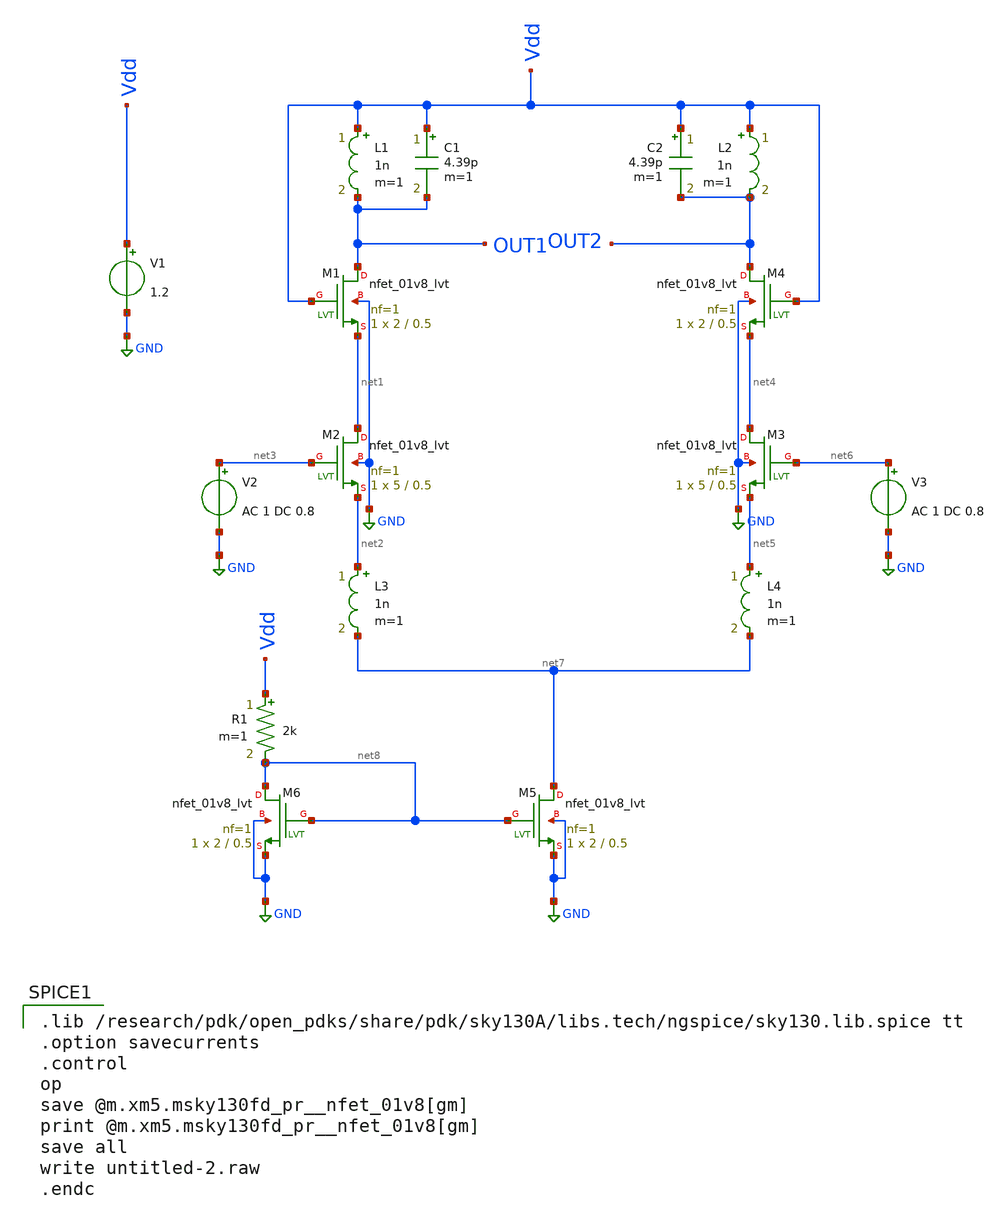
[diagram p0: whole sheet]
** sch_path: skywater_stuff/ECE631_RF_CMOS/untitled-2.sch
**.subckt untitled-2
XM1 OUT1 Vdd net1 GND sky130_fd_pr__nfet_01v8_lvt L=0.5 W=2 nf=1 ad='int((nf+1)/2) * W/nf * 0.29' as='int((nf+2)/2) * W/nf * 0.29'
+ pd='2*int((nf+1)/2) * (W/nf + 0.29)' ps='2*int((nf+2)/2) * (W/nf + 0.29)' nrd='0.29 / W' nrs='0.29 / W'
+ sa=0 sb=0 sd=0 mult=1 m=1
XM2 net1 net3 net2 GND sky130_fd_pr__nfet_01v8_lvt L=0.5 W=5 nf=1 ad='int((nf+1)/2) * W/nf * 0.29' as='int((nf+2)/2) * W/nf * 0.29'
+ pd='2*int((nf+1)/2) * (W/nf + 0.29)' ps='2*int((nf+2)/2) * (W/nf + 0.29)' nrd='0.29 / W' nrs='0.29 / W'
+ sa=0 sb=0 sd=0 mult=1 m=1
V1 Vdd GND 1.2
C1 Vdd OUT1 4.39p m=1
L1 Vdd OUT1 1n m=1
V2 net3 GND AC 1 DC 0.8
XM3 net4 net6 net5 GND sky130_fd_pr__nfet_01v8_lvt L=0.5 W=5 nf=1 ad='int((nf+1)/2) * W/nf * 0.29' as='int((nf+2)/2) * W/nf * 0.29'
+ pd='2*int((nf+1)/2) * (W/nf + 0.29)' ps='2*int((nf+2)/2) * (W/nf + 0.29)' nrd='0.29 / W' nrs='0.29 / W'
+ sa=0 sb=0 sd=0 mult=1 m=1
XM4 OUT2 Vdd net4 GND sky130_fd_pr__nfet_01v8_lvt L=0.5 W=2 nf=1 ad='int((nf+1)/2) * W/nf * 0.29' as='int((nf+2)/2) * W/nf * 0.29'
+ pd='2*int((nf+1)/2) * (W/nf + 0.29)' ps='2*int((nf+2)/2) * (W/nf + 0.29)' nrd='0.29 / W' nrs='0.29 / W'
+ sa=0 sb=0 sd=0 mult=1 m=1
C2 Vdd OUT2 4.39p m=1
L2 Vdd OUT2 1n m=1
L3 net2 net7 1n m=1
L4 net5 net7 1n m=1
V3 net6 GND AC 1 DC 0.8
XM5 net7 net8 GND GND sky130_fd_pr__nfet_01v8_lvt L=0.5 W=2 nf=1 ad='int((nf+1)/2) * W/nf * 0.29' as='int((nf+2)/2) * W/nf * 0.29'
+ pd='2*int((nf+1)/2) * (W/nf + 0.29)' ps='2*int((nf+2)/2) * (W/nf + 0.29)' nrd='0.29 / W' nrs='0.29 / W'
+ sa=0 sb=0 sd=0 mult=1 m=1
XM6 net8 net8 GND GND sky130_fd_pr__nfet_01v8_lvt L=0.5 W=2 nf=1 ad='int((nf+1)/2) * W/nf * 0.29' as='int((nf+2)/2) * W/nf * 0.29'
+ pd='2*int((nf+1)/2) * (W/nf + 0.29)' ps='2*int((nf+2)/2) * (W/nf + 0.29)' nrd='0.29 / W' nrs='0.29 / W'
+ sa=0 sb=0 sd=0 mult=1 m=1
R1 Vdd net8 2k m=1
**** begin user architecture code

.lib /research/pdk/open_pdks/share/pdk/sky130A/libs.tech/ngspice/sky130.lib.spice tt
.option savecurrents
.control
op
save @m.xm5.msky130fd_pr__nfet_01v8[gm]
print @m.xm5.msky130fd_pr__nfet_01v8[gm]
save all
write untitled-2.raw
.endc


**** end user architecture code
**.ends
.GLOBAL GND
.end
